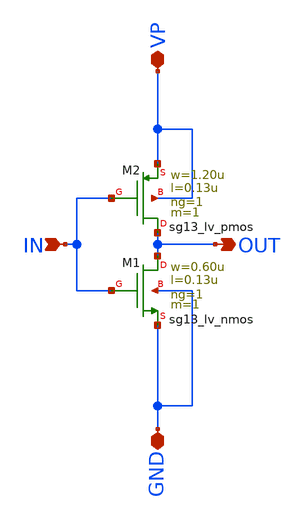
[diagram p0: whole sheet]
** sch_path: schematics/divider/schematics/inverter_x8.sch
**.subckt inverter_x8 IN VP OUT GND
*.ipin IN
*.iopin VP
*.opin OUT
*.iopin GND
XM1 OUT IN GND GND sg13_lv_nmos w=0.60u l=0.13u ng=1 m=1 mm_ok=1
XM2 OUT IN VP VP sg13_lv_pmos w=1.20u l=0.13u ng=1 m=1 mm_ok=1
**.ends
.end
